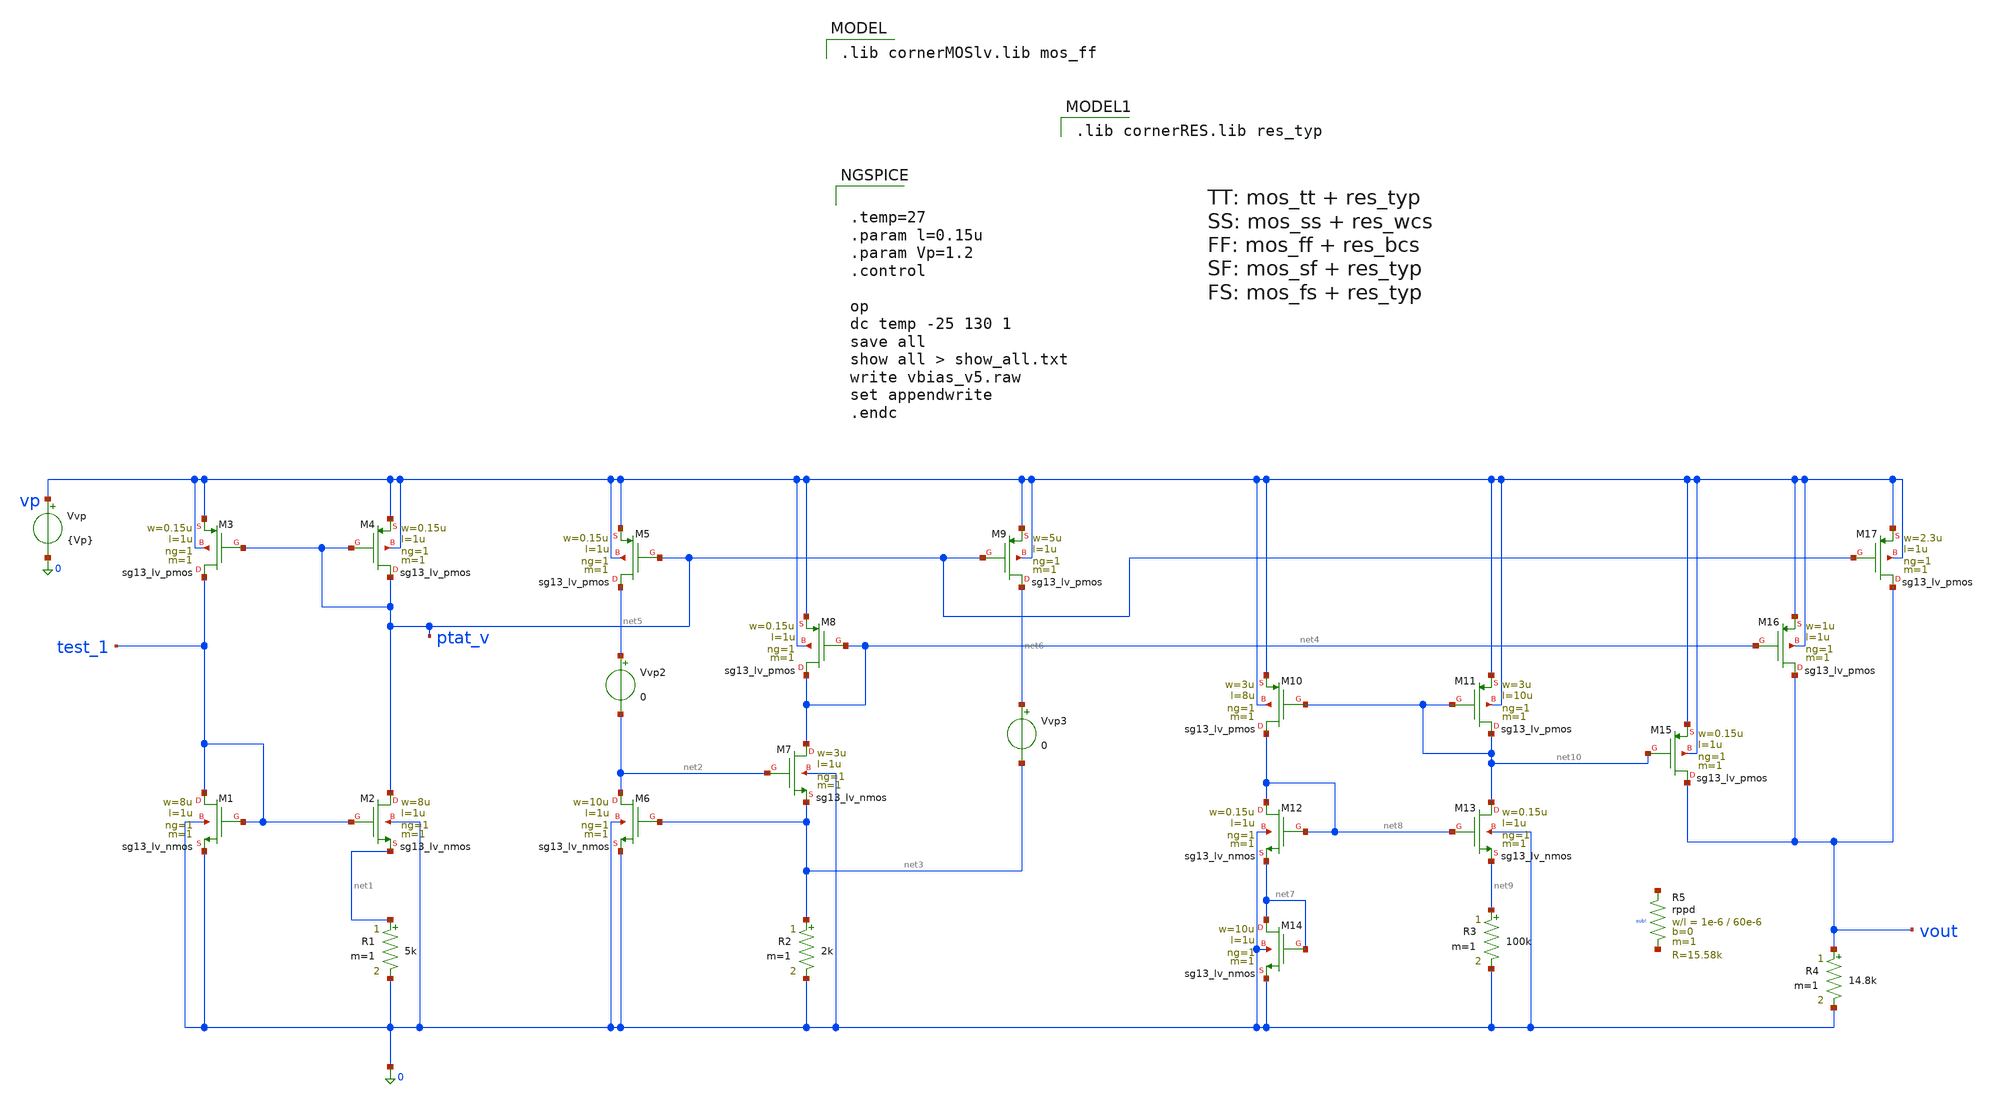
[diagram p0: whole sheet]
** sch_path: PLL0663-main/schematic/xschem/charge_pump/vbias/vbias_v5.sch
**.subckt vbias_v5
XM1 test_1 test_1 0 0 sg13_lv_nmos w=8u l=1u ng=1 m=1 mm_ok=1
XM3 test_1 ptat_v vp vp sg13_lv_pmos w=0.15u l=1u ng=1 m=1 mm_ok=1
XM2 ptat_v test_1 net1 0 sg13_lv_nmos w=8u l=1u ng=1 m=1 mm_ok=1
XM4 ptat_v ptat_v vp vp sg13_lv_pmos w=0.15u l=1u ng=1 m=1 mm_ok=1
R1 net1 0 5k m=1
Vvp vp 0 {Vp}
XM6 net2 net3 0 0 sg13_lv_nmos w=10u l=1u ng=1 m=1 mm_ok=1
XM7 net4 net2 net3 0 sg13_lv_nmos w=3u l=1u ng=1 m=1 mm_ok=1
R2 net3 0 2k m=1
XM5 net5 ptat_v vp vp sg13_lv_pmos w=0.15u l=1u ng=1 m=1 mm_ok=1
XM8 net4 net4 vp vp sg13_lv_pmos w=0.15u l=1u ng=1 m=1 mm_ok=1
XM9 net6 ptat_v vp vp sg13_lv_pmos w=5u l=1u ng=1 m=1 mm_ok=1
XM17 vout ptat_v vp vp sg13_lv_pmos w=2.3u l=1u ng=1 m=1 mm_ok=1
XM16 vout net4 vp vp sg13_lv_pmos w=1u l=1u ng=1 m=1 mm_ok=1
Vvp2 net5 net2 0
Vvp3 net6 net3 0
XM10 net8 net10 vp vp sg13_lv_pmos w=3u l=8u ng=1 m=1 mm_ok=1
XM11 net10 net10 vp vp sg13_lv_pmos w=3u l=10u ng=1 m=1 mm_ok=1
XM12 net8 net8 net7 0 sg13_lv_nmos w=0.15u l=1u ng=1 m=1 mm_ok=1
XM13 net10 net8 net9 0 sg13_lv_nmos w=0.15u l=1u ng=1 m=1 mm_ok=1
XM14 net7 net7 0 0 sg13_lv_nmos w=10u l=1u ng=1 m=1 mm_ok=1
R3 net9 0 100k m=1
XM15 vout net10 vp vp sg13_lv_pmos w=0.15u l=1u ng=1 m=1 mm_ok=1
XR5 net11 net12 sub! rppd w=1e-6 l=60e-6 m=1 b=0 mm_ok=1
R4 vout 0 14.8k m=1
**** begin user architecture code
 .lib cornerMOSlv.lib mos_ff



.temp=27
.param l=0.15u
.param Vp=1.2
.control

op
dc temp -25 130 1
save all
show all > show_all.txt
write vbias_v5.raw
set appendwrite
.endc


 .lib cornerRES.lib res_typ

**** end user architecture code
**.ends
.end
